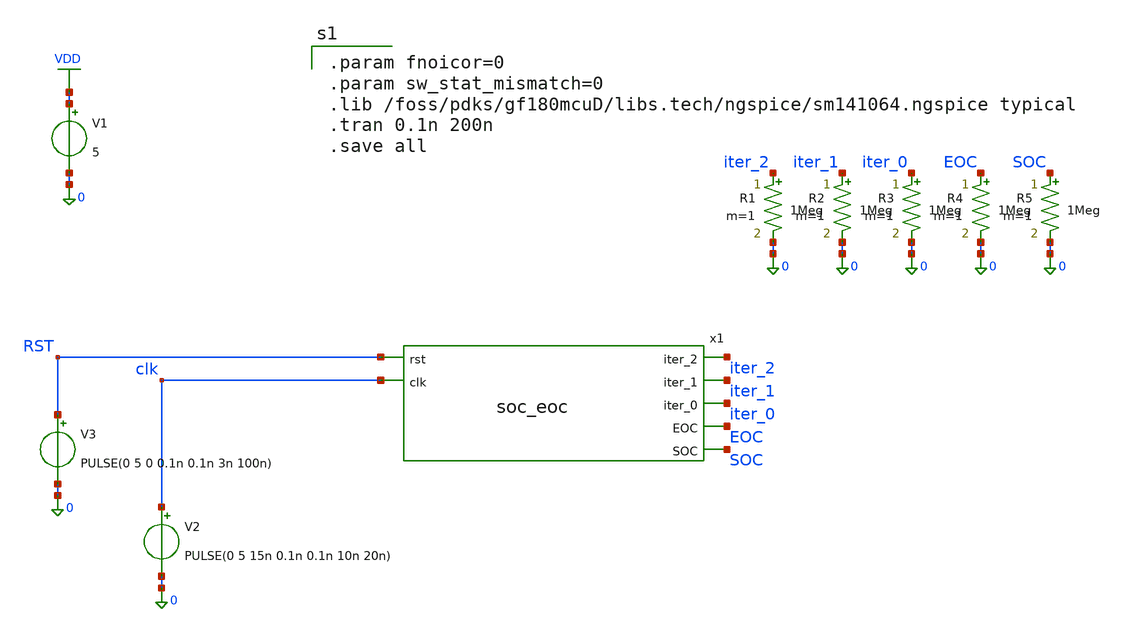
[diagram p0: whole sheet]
** sch_path: xschem/sar_adc/blocks/async_sar/testbench/tb_soc_eoc.sch
**.subckt tb_soc_eoc
x1 iter_2 iter_1 iter_0 RST clk EOC SOC soc_eoc
V1 VDD 0 5
V2 clk 0 PULSE(0 5 15n 0.1n 0.1n 10n 20n)
V3 RST 0 PULSE(0 5 0 0.1n 0.1n 3n 100n)
R1 iter_2 0 1Meg m=1
R2 iter_1 0 1Meg m=1
R3 iter_0 0 1Meg m=1
R4 EOC 0 1Meg m=1
R5 SOC 0 1Meg m=1
**** begin user architecture code

.param fnoicor=0
.param sw_stat_mismatch=0
.lib /foss/pdks/gf180mcuD/libs.tech/ngspice/sm141064.ngspice typical
.tran 0.1n 200n
.save all

**** end user architecture code
**.ends
.GLOBAL VDD
.end
